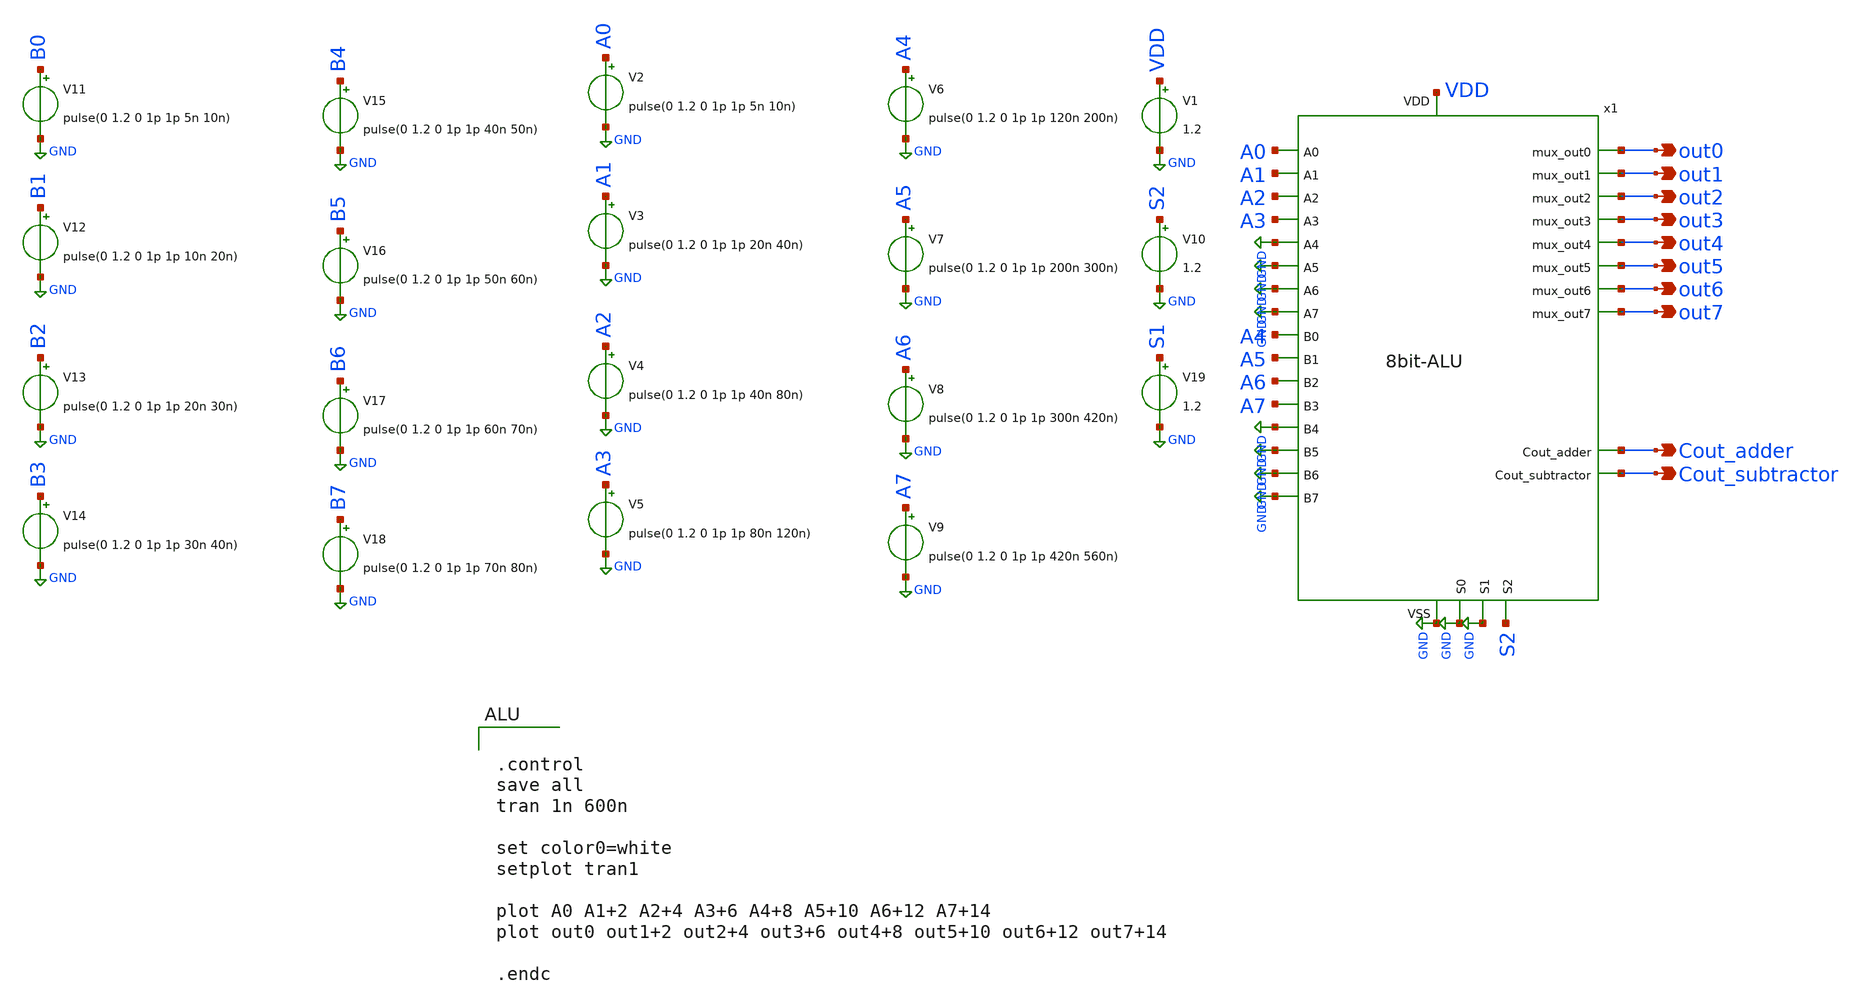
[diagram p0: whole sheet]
** sch_path: 8bit-ALU_tb.sch
**.subckt 8bit-ALU_tb out0 out1 out2 out3 out4 out5 out6 out7 Cout_adder Cout_subtractor
*.opin out0
*.opin out1
*.opin out2
*.opin out3
*.opin out4
*.opin out5
*.opin out6
*.opin out7
*.opin Cout_adder
*.opin Cout_subtractor
x1 VDD GND GND GND GND GND GND A4 A1 A7 A3 GND GND GND A0 A2 A6 A5 Cout_adder Cout_subtractor GND
+ GND S2 out6 out5 out4 out3 out2 out1 out7 out0 8bit-ALU
V1 VDD GND 1.2
V2 A0 GND pulse(0 1.2 0 1p 1p 5n 10n)
V3 A1 GND pulse(0 1.2 0 1p 1p 20n 40n)
V4 A2 GND pulse(0 1.2 0 1p 1p 40n 80n)
V5 A3 GND pulse(0 1.2 0 1p 1p 80n 120n)
V6 A4 GND pulse(0 1.2 0 1p 1p 120n 200n)
V7 A5 GND pulse(0 1.2 0 1p 1p 200n 300n)
V8 A6 GND pulse(0 1.2 0 1p 1p 300n 420n)
V9 A7 GND pulse(0 1.2 0 1p 1p 420n 560n)
V10 S2 GND 1.2
V11 B0 GND pulse(0 1.2 0 1p 1p 5n 10n)
V12 B1 GND pulse(0 1.2 0 1p 1p 10n 20n)
V13 B2 GND pulse(0 1.2 0 1p 1p 20n 30n)
V14 B3 GND pulse(0 1.2 0 1p 1p 30n 40n)
V15 B4 GND pulse(0 1.2 0 1p 1p 40n 50n)
V16 B5 GND pulse(0 1.2 0 1p 1p 50n 60n)
V17 B6 GND pulse(0 1.2 0 1p 1p 60n 70n)
V18 B7 GND pulse(0 1.2 0 1p 1p 70n 80n)
V19 S1 GND 1.2
**** begin user architecture code

** opencircuitdesign pdks install
.lib $::SKYWATER_MODELS/sky130.lib.spice tt_mm




.control
save all
tran 1n 600n

set color0=white
setplot tran1

plot A0 A1+2 A2+4 A3+6 A4+8 A5+10 A6+12 A7+14
plot out0 out1+2 out2+4 out3+6 out4+8 out5+10 out6+12 out7+14

.endc


**** end user architecture code
**.ends
.GLOBAL GND
.end
